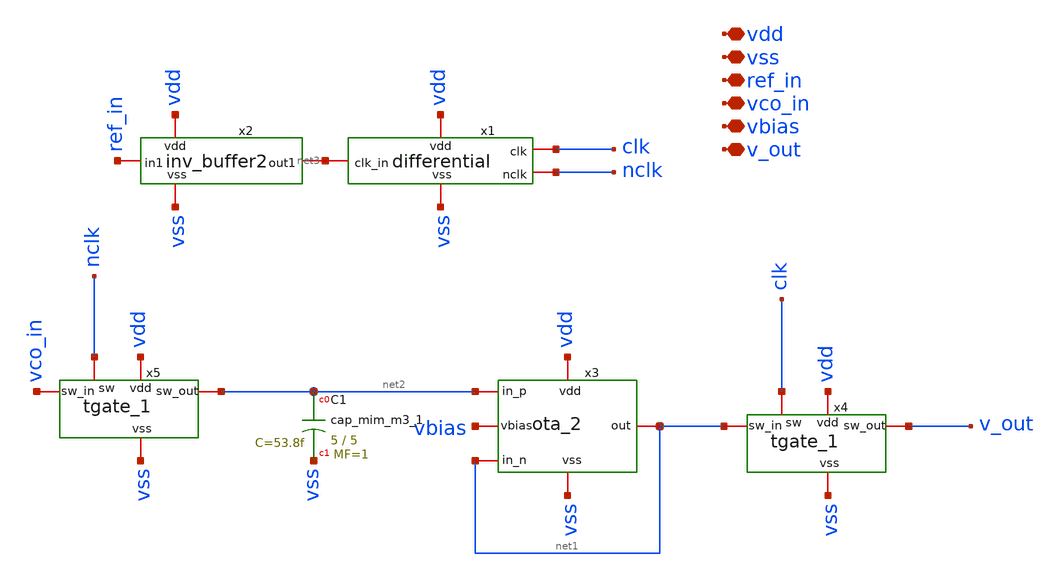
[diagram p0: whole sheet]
** sch_path: xschem/sspd.sch
**.subckt sspd vdd vss ref_in vco_in vbias v_out
*.iopin vdd
*.iopin vss
*.iopin ref_in
*.iopin vco_in
*.iopin vbias
*.iopin v_out
x2 vdd vss net3 ref_in inv_buffer2
x1 vdd vss net3 clk nclk differential
x3 vdd vss net2 net1 net1 vbias ota_2
XC1 net2 vss sky130_fd_pr__cap_mim_m3_1 W=5 L=5 MF=1 m=1
x4 v_out net1 vss vdd clk tgate_1
x5 net2 vco_in vss vdd nclk tgate_1
**.ends

* expanding   symbol:  inv_buffer2.sym # of pins=4
** sym_path: xschem/inv_buffer2.sym
** sch_path: xschem/inv_buffer2.sch
.subckt inv_buffer2 vdd vss out1 in1
*.iopin in1
*.iopin out1
*.iopin vdd
*.iopin vss
XM4 out1 net1 vss vss sky130_fd_pr__nfet_01v8 L=0.15 W=2.8 nf=4 ad='int((nf+1)/2) * W/nf * 0.29' as='int((nf+2)/2) * W/nf * 0.29'
+ pd='2*int((nf+1)/2) * (W/nf + 0.29)' ps='2*int((nf+2)/2) * (W/nf + 0.29)' nrd='0.29 / W' nrs='0.29 / W'
+ sa=0 sb=0 sd=0 mult=1 m=1
XM1 out1 net1 vdd vdd sky130_fd_pr__pfet_01v8 L=0.15 W=5.6 nf=8 ad='int((nf+1)/2) * W/nf * 0.29' as='int((nf+2)/2) * W/nf * 0.29'
+ pd='2*int((nf+1)/2) * (W/nf + 0.29)' ps='2*int((nf+2)/2) * (W/nf + 0.29)' nrd='0.29 / W' nrs='0.29 / W'
+ sa=0 sb=0 sd=0 mult=1 m=1
XM5 vdd vdd vdd vdd sky130_fd_pr__pfet_01v8 L=0.15 W=1.4 nf=2 ad='int((nf+1)/2) * W/nf * 0.29' as='int((nf+2)/2) * W/nf * 0.29'
+ pd='2*int((nf+1)/2) * (W/nf + 0.29)' ps='2*int((nf+2)/2) * (W/nf + 0.29)' nrd='0.29 / W' nrs='0.29 / W'
+ sa=0 sb=0 sd=0 mult=1 m=1
XM6 vss vss vss vss sky130_fd_pr__nfet_01v8 L=0.15 W=1.4 nf=2 ad='int((nf+1)/2) * W/nf * 0.29' as='int((nf+2)/2) * W/nf * 0.29'
+ pd='2*int((nf+1)/2) * (W/nf + 0.29)' ps='2*int((nf+2)/2) * (W/nf + 0.29)' nrd='0.29 / W' nrs='0.29 / W'
+ sa=0 sb=0 sd=0 mult=1 m=1
x1 vdd in1 net1 vss inv_simple1
.ends


* expanding   symbol:  differential.sym # of pins=5
** sym_path: xschem/differential.sym
** sch_path: xschem/differential.sch
.subckt differential vdd vss clk_in clk nclk
*.iopin vdd
*.iopin vss
*.iopin clk_in
*.iopin clk
*.iopin nclk
XM2 net1 vdd vss vss sky130_fd_pr__nfet_01v8 L=0.15 W=1.4 nf=2 ad='int((nf+1)/2) * W/nf * 0.29' as='int((nf+2)/2) * W/nf * 0.29'
+ pd='2*int((nf+1)/2) * (W/nf + 0.29)' ps='2*int((nf+2)/2) * (W/nf + 0.29)' nrd='0.29 / W' nrs='0.29 / W'
+ sa=0 sb=0 sd=0 mult=1 m=1
XM7 net2 vss vdd vdd sky130_fd_pr__pfet_01v8 L=0.15 W=2.8 nf=4 ad='int((nf+1)/2) * W/nf * 0.29' as='int((nf+2)/2) * W/nf * 0.29'
+ pd='2*int((nf+1)/2) * (W/nf + 0.29)' ps='2*int((nf+2)/2) * (W/nf + 0.29)' nrd='0.29 / W' nrs='0.29 / W'
+ sa=0 sb=0 sd=0 mult=1 m=1
x1 vdd clk_in net4 vss inv_simple1
x2 vdd net4 net5 vss inv_simple1
x3 vdd net5 nclk vss inv_simple1
x4 vdd net3 clk vss inv_simple1
XM1 net2 net2 net2 vdd sky130_fd_pr__pfet_01v8 L=0.15 W=2.8 nf=4 ad='int((nf+1)/2) * W/nf * 0.29' as='int((nf+2)/2) * W/nf * 0.29'
+ pd='2*int((nf+1)/2) * (W/nf + 0.29)' ps='2*int((nf+2)/2) * (W/nf + 0.29)' nrd='0.29 / W' nrs='0.29 / W'
+ sa=0 sb=0 sd=0 mult=1 m=1
XM3 net1 net1 net1 vss sky130_fd_pr__nfet_01v8 L=0.15 W=2.8 nf=4 ad='int((nf+1)/2) * W/nf * 0.29' as='int((nf+2)/2) * W/nf * 0.29'
+ pd='2*int((nf+1)/2) * (W/nf + 0.29)' ps='2*int((nf+2)/2) * (W/nf + 0.29)' nrd='0.29 / W' nrs='0.29 / W'
+ sa=0 sb=0 sd=0 mult=1 m=1
XM4 net3 clk_in net1 vss sky130_fd_pr__nfet_01v8 L=0.15 W=1.4 nf=2 ad='int((nf+1)/2) * W/nf * 0.29' as='int((nf+2)/2) * W/nf * 0.29'
+ pd='2*int((nf+1)/2) * (W/nf + 0.29)' ps='2*int((nf+2)/2) * (W/nf + 0.29)' nrd='0.29 / W' nrs='0.29 / W'
+ sa=0 sb=0 sd=0 mult=1 m=1
XM5 net3 clk_in net2 vdd sky130_fd_pr__pfet_01v8 L=0.15 W=2.8 nf=4 ad='int((nf+1)/2) * W/nf * 0.29' as='int((nf+2)/2) * W/nf * 0.29'
+ pd='2*int((nf+1)/2) * (W/nf + 0.29)' ps='2*int((nf+2)/2) * (W/nf + 0.29)' nrd='0.29 / W' nrs='0.29 / W'
+ sa=0 sb=0 sd=0 mult=1 m=1
.ends


* expanding   symbol:  ota_2.sym # of pins=6
** sym_path: xschem/ota_2.sym
** sch_path: xschem/ota_2.sch
.subckt ota_2 vdd vss in_p in_n out vbias
*.iopin vdd
*.iopin vss
*.iopin in_p
*.iopin in_n
*.iopin out
*.iopin vbias
XM1 net3 in_n net2 net2 sky130_fd_pr__nfet_01v8 L=0.15 W=1.4 nf=2 ad='int((nf+1)/2) * W/nf * 0.29' as='int((nf+2)/2) * W/nf * 0.29'
+ pd='2*int((nf+1)/2) * (W/nf + 0.29)' ps='2*int((nf+2)/2) * (W/nf + 0.29)' nrd='0.29 / W' nrs='0.29 / W'
+ sa=0 sb=0 sd=0 mult=1 m=1
XM3 net1 net3 vdd vdd sky130_fd_pr__pfet_01v8 L=0.15 W=14.0 nf=20 ad='int((nf+1)/2) * W/nf * 0.29' as='int((nf+2)/2) * W/nf * 0.29'
+ pd='2*int((nf+1)/2) * (W/nf + 0.29)' ps='2*int((nf+2)/2) * (W/nf + 0.29)' nrd='0.29 / W' nrs='0.29 / W'
+ sa=0 sb=0 sd=0 mult=1 m=1
XM2 out net4 vdd vdd sky130_fd_pr__pfet_01v8 L=0.15 W=14.0 nf=20 ad='int((nf+1)/2) * W/nf * 0.29' as='int((nf+2)/2) * W/nf * 0.29'
+ pd='2*int((nf+1)/2) * (W/nf + 0.29)' ps='2*int((nf+2)/2) * (W/nf + 0.29)' nrd='0.29 / W' nrs='0.29 / W'
+ sa=0 sb=0 sd=0 mult=1 m=1
XM4 net4 in_p net2 net2 sky130_fd_pr__nfet_01v8 L=0.15 W=1.4 nf=2 ad='int((nf+1)/2) * W/nf * 0.29' as='int((nf+2)/2) * W/nf * 0.29'
+ pd='2*int((nf+1)/2) * (W/nf + 0.29)' ps='2*int((nf+2)/2) * (W/nf + 0.29)' nrd='0.29 / W' nrs='0.29 / W'
+ sa=0 sb=0 sd=0 mult=1 m=1
XM12 net1 net1 vss vss sky130_fd_pr__nfet_01v8 L=0.15 W=7.0 nf=10 ad='int((nf+1)/2) * W/nf * 0.29' as='int((nf+2)/2) * W/nf * 0.29'
+ pd='2*int((nf+1)/2) * (W/nf + 0.29)' ps='2*int((nf+2)/2) * (W/nf + 0.29)' nrd='0.29 / W' nrs='0.29 / W'
+ sa=0 sb=0 sd=0 mult=1 m=1
XM13 out net1 vss vss sky130_fd_pr__nfet_01v8 L=0.15 W=7.0 nf=10 ad='int((nf+1)/2) * W/nf * 0.29' as='int((nf+2)/2) * W/nf * 0.29'
+ pd='2*int((nf+1)/2) * (W/nf + 0.29)' ps='2*int((nf+2)/2) * (W/nf + 0.29)' nrd='0.29 / W' nrs='0.29 / W'
+ sa=0 sb=0 sd=0 mult=1 m=1
XM14 net3 net3 vdd vdd sky130_fd_pr__pfet_01v8 L=0.15 W=1.4 nf=2 ad='int((nf+1)/2) * W/nf * 0.29' as='int((nf+2)/2) * W/nf * 0.29'
+ pd='2*int((nf+1)/2) * (W/nf + 0.29)' ps='2*int((nf+2)/2) * (W/nf + 0.29)' nrd='0.29 / W' nrs='0.29 / W'
+ sa=0 sb=0 sd=0 mult=1 m=1
XM15 net4 net4 vdd vdd sky130_fd_pr__pfet_01v8 L=0.15 W=1.4 nf=2 ad='int((nf+1)/2) * W/nf * 0.29' as='int((nf+2)/2) * W/nf * 0.29'
+ pd='2*int((nf+1)/2) * (W/nf + 0.29)' ps='2*int((nf+2)/2) * (W/nf + 0.29)' nrd='0.29 / W' nrs='0.29 / W'
+ sa=0 sb=0 sd=0 mult=1 m=1
XM16 net2 vbias vss vss sky130_fd_pr__nfet_01v8 L=0.15 W=4.2 nf=6 ad='int((nf+1)/2) * W/nf * 0.29' as='int((nf+2)/2) * W/nf * 0.29'
+ pd='2*int((nf+1)/2) * (W/nf + 0.29)' ps='2*int((nf+2)/2) * (W/nf + 0.29)' nrd='0.29 / W' nrs='0.29 / W'
+ sa=0 sb=0 sd=0 mult=1 m=1
XM5 vdd vdd vdd vdd sky130_fd_pr__pfet_01v8 L=0.15 W=2.8 nf=4 ad='int((nf+1)/2) * W/nf * 0.29' as='int((nf+2)/2) * W/nf * 0.29'
+ pd='2*int((nf+1)/2) * (W/nf + 0.29)' ps='2*int((nf+2)/2) * (W/nf + 0.29)' nrd='0.29 / W' nrs='0.29 / W'
+ sa=0 sb=0 sd=0 mult=1 m=1
XM6 vss vss vss vss sky130_fd_pr__nfet_01v8 L=0.15 W=4.2 nf=6 ad='int((nf+1)/2) * W/nf * 0.29' as='int((nf+2)/2) * W/nf * 0.29'
+ pd='2*int((nf+1)/2) * (W/nf + 0.29)' ps='2*int((nf+2)/2) * (W/nf + 0.29)' nrd='0.29 / W' nrs='0.29 / W'
+ sa=0 sb=0 sd=0 mult=1 m=1
XM7 net2 net2 net2 net2 sky130_fd_pr__nfet_01v8 L=0.15 W=2.8 nf=2 ad='int((nf+1)/2) * W/nf * 0.29' as='int((nf+2)/2) * W/nf * 0.29'
+ pd='2*int((nf+1)/2) * (W/nf + 0.29)' ps='2*int((nf+2)/2) * (W/nf + 0.29)' nrd='0.29 / W' nrs='0.29 / W'
+ sa=0 sb=0 sd=0 mult=1 m=1
.ends


* expanding   symbol:  tgate_1.sym # of pins=5
** sym_path: xschem/tgate_1.sym
** sch_path: xschem/tgate_1.sch
.subckt tgate_1 sw_out sw_in vss vdd sw
*.iopin sw_in
*.iopin vdd
*.iopin vss
*.iopin sw
*.iopin sw_out
XM17 sw_out sw sw_in vdd sky130_fd_pr__pfet_01v8 L=0.15 W=1.4 nf=2 ad='int((nf+1)/2) * W/nf * 0.29' as='int((nf+2)/2) * W/nf * 0.29'
+ pd='2*int((nf+1)/2) * (W/nf + 0.29)' ps='2*int((nf+2)/2) * (W/nf + 0.29)' nrd='0.29 / W' nrs='0.29 / W'
+ sa=0 sb=0 sd=0 mult=1 m=1
XM18 sw_in net1 sw_out vss sky130_fd_pr__nfet_01v8 L=0.15 W=1.4 nf=2 ad='int((nf+1)/2) * W/nf * 0.29'
+ as='int((nf+2)/2) * W/nf * 0.29' pd='2*int((nf+1)/2) * (W/nf + 0.29)' ps='2*int((nf+2)/2) * (W/nf + 0.29)'
+ nrd='0.29 / W' nrs='0.29 / W' sa=0 sb=0 sd=0 mult=1 m=1
x1 vdd sw net1 vss inv_simple1
XM1 sw_out sw_out sw_out vdd sky130_fd_pr__pfet_01v8 L=0.15 W=1.4 nf=2 ad='int((nf+1)/2) * W/nf * 0.29'
+ as='int((nf+2)/2) * W/nf * 0.29' pd='2*int((nf+1)/2) * (W/nf + 0.29)' ps='2*int((nf+2)/2) * (W/nf + 0.29)'
+ nrd='0.29 / W' nrs='0.29 / W' sa=0 sb=0 sd=0 mult=1 m=1
XM2 sw_out sw_out sw_out vss sky130_fd_pr__nfet_01v8 L=0.15 W=1.4 nf=2 ad='int((nf+1)/2) * W/nf * 0.29'
+ as='int((nf+2)/2) * W/nf * 0.29' pd='2*int((nf+1)/2) * (W/nf + 0.29)' ps='2*int((nf+2)/2) * (W/nf + 0.29)'
+ nrd='0.29 / W' nrs='0.29 / W' sa=0 sb=0 sd=0 mult=1 m=1
.ends


* expanding   symbol:  inv_simple1.sym # of pins=4
** sym_path: xschem/inv_simple1.sym
** sch_path: xschem/inv_simple1.sch
.subckt inv_simple1 vdd in out vss
*.iopin in
*.iopin vdd
*.iopin vss
*.iopin out
XM19 out in vss vss sky130_fd_pr__nfet_01v8 L=0.15 W=1.4 nf=1 ad='int((nf+1)/2) * W/nf * 0.29' as='int((nf+2)/2) * W/nf * 0.29'
+ pd='2*int((nf+1)/2) * (W/nf + 0.29)' ps='2*int((nf+2)/2) * (W/nf + 0.29)' nrd='0.29 / W' nrs='0.29 / W'
+ sa=0 sb=0 sd=0 mult=1 m=1
XM20 out in vdd vdd sky130_fd_pr__pfet_01v8 L=0.15 W=2.8 nf=1 ad='int((nf+1)/2) * W/nf * 0.29' as='int((nf+2)/2) * W/nf * 0.29'
+ pd='2*int((nf+1)/2) * (W/nf + 0.29)' ps='2*int((nf+2)/2) * (W/nf + 0.29)' nrd='0.29 / W' nrs='0.29 / W'
+ sa=0 sb=0 sd=0 mult=1 m=1
XM1 vdd vdd vdd vdd sky130_fd_pr__pfet_01v8 L=0.15 W=1.4 nf=1 ad='int((nf+1)/2) * W/nf * 0.29' as='int((nf+2)/2) * W/nf * 0.29'
+ pd='2*int((nf+1)/2) * (W/nf + 0.29)' ps='2*int((nf+2)/2) * (W/nf + 0.29)' nrd='0.29 / W' nrs='0.29 / W'
+ sa=0 sb=0 sd=0 mult=1 m=1
XM2 vss vss vss vss sky130_fd_pr__nfet_01v8 L=0.15 W=1.4 nf=1 ad='int((nf+1)/2) * W/nf * 0.29' as='int((nf+2)/2) * W/nf * 0.29'
+ pd='2*int((nf+1)/2) * (W/nf + 0.29)' ps='2*int((nf+2)/2) * (W/nf + 0.29)' nrd='0.29 / W' nrs='0.29 / W'
+ sa=0 sb=0 sd=0 mult=1 m=1
.ends

.end
